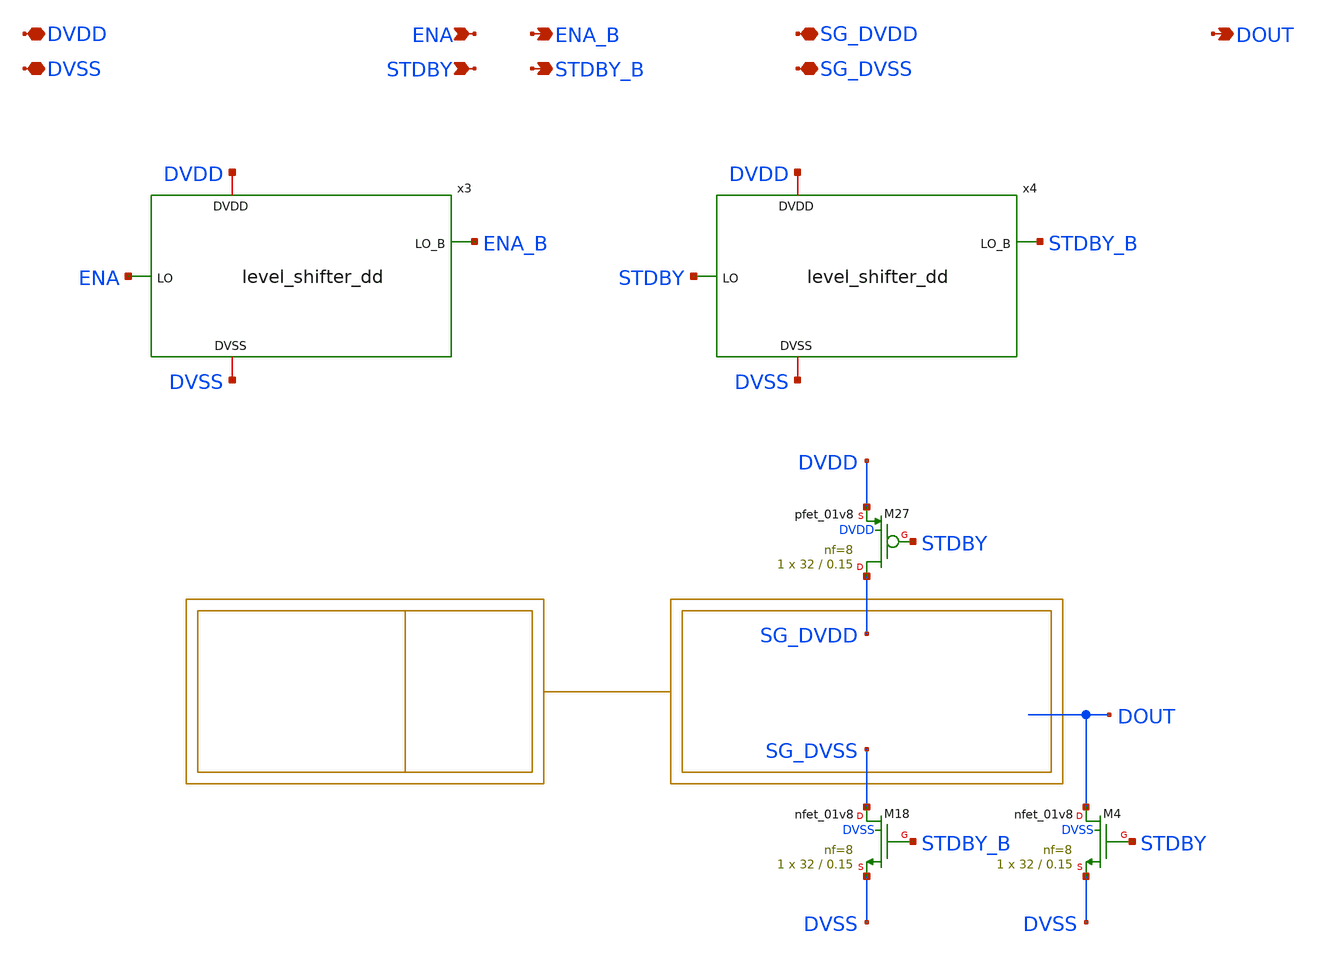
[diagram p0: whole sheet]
** sch_path: xschem/power_gating_dd.sch
**.subckt power_gating_dd DVDD DVSS ENA STDBY DOUT SG_DVDD SG_DVSS ENA_B STDBY_B
*.iopin DVDD
*.iopin DVSS
*.ipin ENA
*.ipin STDBY
*.opin DOUT
*.iopin SG_DVDD
*.iopin SG_DVSS
*.opin ENA_B
*.opin STDBY_B
x3 ENA_B DVDD ENA DVSS level_shifter_dd
x4 STDBY_B DVDD STDBY DVSS level_shifter_dd
XM18 SG_DVSS STDBY_B DVSS DVSS sky130_fd_pr__nfet_01v8 L=0.15 W=32 nf=8 ad='int((nf+1)/2) * W/nf * 0.29'
+ as='int((nf+2)/2) * W/nf * 0.29' pd='2*int((nf+1)/2) * (W/nf + 0.29)' ps='2*int((nf+2)/2) * (W/nf + 0.29)'
+ nrd='0.29 / W' nrs='0.29 / W' sa=0 sb=0 sd=0 mult=1 m=1
XM27 SG_DVDD STDBY DVDD DVDD sky130_fd_pr__pfet_01v8 L=0.15 W=32 nf=8 ad='int((8 + 1)/2) * 32 / 8 * 0.29'
+ as='int((8 + 2)/2) * 32 / 8 * 0.29' pd='2*int((8 + 1)/2) * (32 / 8 + 0.29)' ps='2*int((8 + 2)/2) * (32 / 8 + 0.29)'
+ nrd='0.29 / 32 ' nrs='0.29 / 32 ' sa=0 sb=0 sd=0 mult=1 m=1
XM4 DOUT STDBY DVSS DVSS sky130_fd_pr__nfet_01v8 L=0.15 W=32 nf=8 ad='int((nf+1)/2) * W/nf * 0.29' as='int((nf+2)/2) * W/nf * 0.29'
+ pd='2*int((nf+1)/2) * (W/nf + 0.29)' ps='2*int((nf+2)/2) * (W/nf + 0.29)' nrd='0.29 / W' nrs='0.29 / W'
+ sa=0 sb=0 sd=0 mult=1 m=1
**.ends

* expanding   symbol:  level_shifter_dd.sym # of pins=4
** sym_path: xschem/level_shifter_dd.sym
** sch_path: xschem/level_shifter_dd.sch
.subckt level_shifter_dd LO_B DVDD LO DVSS
*.iopin DVDD
*.iopin DVSS
*.ipin LO
*.opin LO_B
XM18 LO_B LO DVSS DVSS sky130_fd_pr__nfet_01v8 L=0.15 W=1 nf=1 ad='int((nf+1)/2) * W/nf * 0.29' as='int((nf+2)/2) * W/nf * 0.29'
+ pd='2*int((nf+1)/2) * (W/nf + 0.29)' ps='2*int((nf+2)/2) * (W/nf + 0.29)' nrd='0.29 / W' nrs='0.29 / W'
+ sa=0 sb=0 sd=0 mult=1 m=1
XM27 LO_B LO DVDD DVDD sky130_fd_pr__pfet_01v8 L=0.15 W=1 nf=1 ad='int((1 + 1)/2) * 1 / 1 * 0.29' as='int((1 + 2)/2) * 1 / 1 * 0.29'
+ pd='2*int((1 + 1)/2) * (1 / 1 + 0.29)' ps='2*int((1 + 2)/2) * (1 / 1 + 0.29)' nrd='0.29 / 1 ' nrs='0.29 / 1 '
+ sa=0 sb=0 sd=0 mult=1 m=1
.ends

.end
